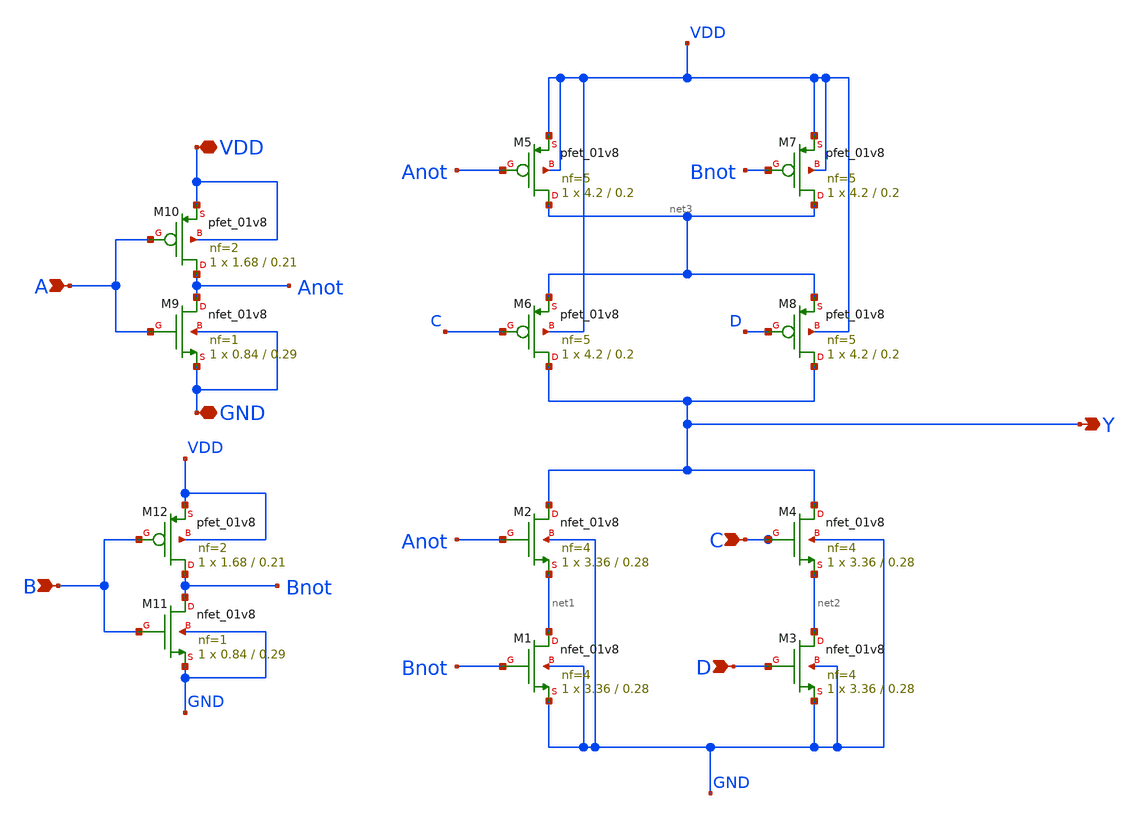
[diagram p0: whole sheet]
** sch_path: cells/MAOI4X4/schematic/maoi4x4.sch
**.subckt maoi4x4 A VDD GND B Y D C
*.ipin A
*.iopin VDD
*.iopin GND
*.ipin B
*.opin Y
*.ipin D
*.ipin C
XM9 Anot A GND GND sky130_fd_pr__nfet_01v8 L=0.29 W=0.84 nf=1 ad='int((1 + 1)/2) * 0.84 / 1 * 0.29' as='int((1 + 2)/2) * 0.84 / 1 * 0.29'
+ pd='2*int((1 + 1)/2) * (0.84 / 1 + 0.29)' ps='2*int((1 + 2)/2) * (0.84 / 1 + 0.29)' nrd='0.29 / 0.84 '
+ nrs='0.29 / 0.84 ' sa=0 sb=0 sd=0 mult=1 m=1
XM2 Y Anot net1 GND sky130_fd_pr__nfet_01v8 L=0.28 W=3.36 nf=4 ad='int((4 + 1)/2) * 3.36 / 4 * 0.29'
+ as='int((4 + 2)/2) * 3.36 / 4 * 0.29' pd='2*int((4 + 1)/2) * (3.36 / 4 + 0.29)' ps='2*int((4 + 2)/2) * (3.36 / 4 + 0.29)'
+ nrd='0.29 / 3.36 ' nrs='0.29 / 3.36 ' sa=0 sb=0 sd=0 mult=1 m=1
XM5 net3 Anot VDD VDD sky130_fd_pr__pfet_01v8 L=0.2 W=4.2 nf=5 ad='int((5 + 1)/2) * 4.2 / 5 * 0.29' as='int((5 + 2)/2) * 4.2 / 5 * 0.29'
+ pd='2*int((5 + 1)/2) * (4.2 / 5 + 0.29)' ps='2*int((5 + 2)/2) * (4.2 / 5 + 0.29)' nrd='0.29 / 4.2 ' nrs='0.29 / 4.2 '
+ sa=0 sb=0 sd=0 mult=1 m=1
XM10 Anot A VDD VDD sky130_fd_pr__pfet_01v8 L=0.21 W=1.68 nf=2 ad='int((2 + 1)/2) * 1.68 / 2 * 0.29'
+ as='int((2 + 2)/2) * 1.68 / 2 * 0.29' pd='2*int((2 + 1)/2) * (1.68 / 2 + 0.29)' ps='2*int((2 + 2)/2) * (1.68 / 2 + 0.29)'
+ nrd='0.29 / 1.68 ' nrs='0.29 / 1.68 ' sa=0 sb=0 sd=0 mult=1 m=1
XM7 net3 Bnot VDD VDD sky130_fd_pr__pfet_01v8 L=0.2 W=4.2 nf=5 ad='int((5 + 1)/2) * 4.2 / 5 * 0.29' as='int((5 + 2)/2) * 4.2 / 5 * 0.29'
+ pd='2*int((5 + 1)/2) * (4.2 / 5 + 0.29)' ps='2*int((5 + 2)/2) * (4.2 / 5 + 0.29)' nrd='0.29 / 4.2 ' nrs='0.29 / 4.2 '
+ sa=0 sb=0 sd=0 mult=1 m=1
XM8 Y D net3 VDD sky130_fd_pr__pfet_01v8 L=0.2 W=4.2 nf=5 ad='int((5 + 1)/2) * 4.2 / 5 * 0.29' as='int((5 + 2)/2) * 4.2 / 5 * 0.29'
+ pd='2*int((5 + 1)/2) * (4.2 / 5 + 0.29)' ps='2*int((5 + 2)/2) * (4.2 / 5 + 0.29)' nrd='0.29 / 4.2 ' nrs='0.29 / 4.2 '
+ sa=0 sb=0 sd=0 mult=1 m=1
XM6 Y C net3 VDD sky130_fd_pr__pfet_01v8 L=0.2 W=4.2 nf=5 ad='int((5 + 1)/2) * 4.2 / 5 * 0.29' as='int((5 + 2)/2) * 4.2 / 5 * 0.29'
+ pd='2*int((5 + 1)/2) * (4.2 / 5 + 0.29)' ps='2*int((5 + 2)/2) * (4.2 / 5 + 0.29)' nrd='0.29 / 4.2 ' nrs='0.29 / 4.2 '
+ sa=0 sb=0 sd=0 mult=1 m=1
XM4 Y C net2 GND sky130_fd_pr__nfet_01v8 L=0.28 W=3.36 nf=4 ad='int((4 + 1)/2) * 3.36 / 4 * 0.29' as='int((4 + 2)/2) * 3.36 / 4 * 0.29'
+ pd='2*int((4 + 1)/2) * (3.36 / 4 + 0.29)' ps='2*int((4 + 2)/2) * (3.36 / 4 + 0.29)' nrd='0.29 / 3.36 '
+ nrs='0.29 / 3.36 ' sa=0 sb=0 sd=0 mult=1 m=1
XM3 net2 D GND GND sky130_fd_pr__nfet_01v8 L=0.28 W=3.36 nf=4 ad='int((4 + 1)/2) * 3.36 / 4 * 0.29' as='int((4 + 2)/2) * 3.36 / 4 * 0.29'
+ pd='2*int((4 + 1)/2) * (3.36 / 4 + 0.29)' ps='2*int((4 + 2)/2) * (3.36 / 4 + 0.29)' nrd='0.29 / 3.36 '
+ nrs='0.29 / 3.36 ' sa=0 sb=0 sd=0 mult=1 m=1
XM1 net1 Bnot GND GND sky130_fd_pr__nfet_01v8 L=0.28 W=3.36 nf=4 ad='int((4 + 1)/2) * 3.36 / 4 * 0.29'
+ as='int((4 + 2)/2) * 3.36 / 4 * 0.29' pd='2*int((4 + 1)/2) * (3.36 / 4 + 0.29)' ps='2*int((4 + 2)/2) * (3.36 / 4 + 0.29)'
+ nrd='0.29 / 3.36 ' nrs='0.29 / 3.36 ' sa=0 sb=0 sd=0 mult=1 m=1
XM11 Bnot B GND GND sky130_fd_pr__nfet_01v8 L=0.29 W=0.84 nf=1 ad='int((1 + 1)/2) * 0.84 / 1 * 0.29'
+ as='int((1 + 2)/2) * 0.84 / 1 * 0.29' pd='2*int((1 + 1)/2) * (0.84 / 1 + 0.29)' ps='2*int((1 + 2)/2) * (0.84 / 1 + 0.29)'
+ nrd='0.29 / 0.84 ' nrs='0.29 / 0.84 ' sa=0 sb=0 sd=0 mult=1 m=1
XM12 Bnot B VDD VDD sky130_fd_pr__pfet_01v8 L=0.21 W=1.68 nf=2 ad='int((2 + 1)/2) * 1.68 / 2 * 0.29'
+ as='int((2 + 2)/2) * 1.68 / 2 * 0.29' pd='2*int((2 + 1)/2) * (1.68 / 2 + 0.29)' ps='2*int((2 + 2)/2) * (1.68 / 2 + 0.29)'
+ nrd='0.29 / 1.68 ' nrs='0.29 / 1.68 ' sa=0 sb=0 sd=0 mult=1 m=1
**.ends
.end
